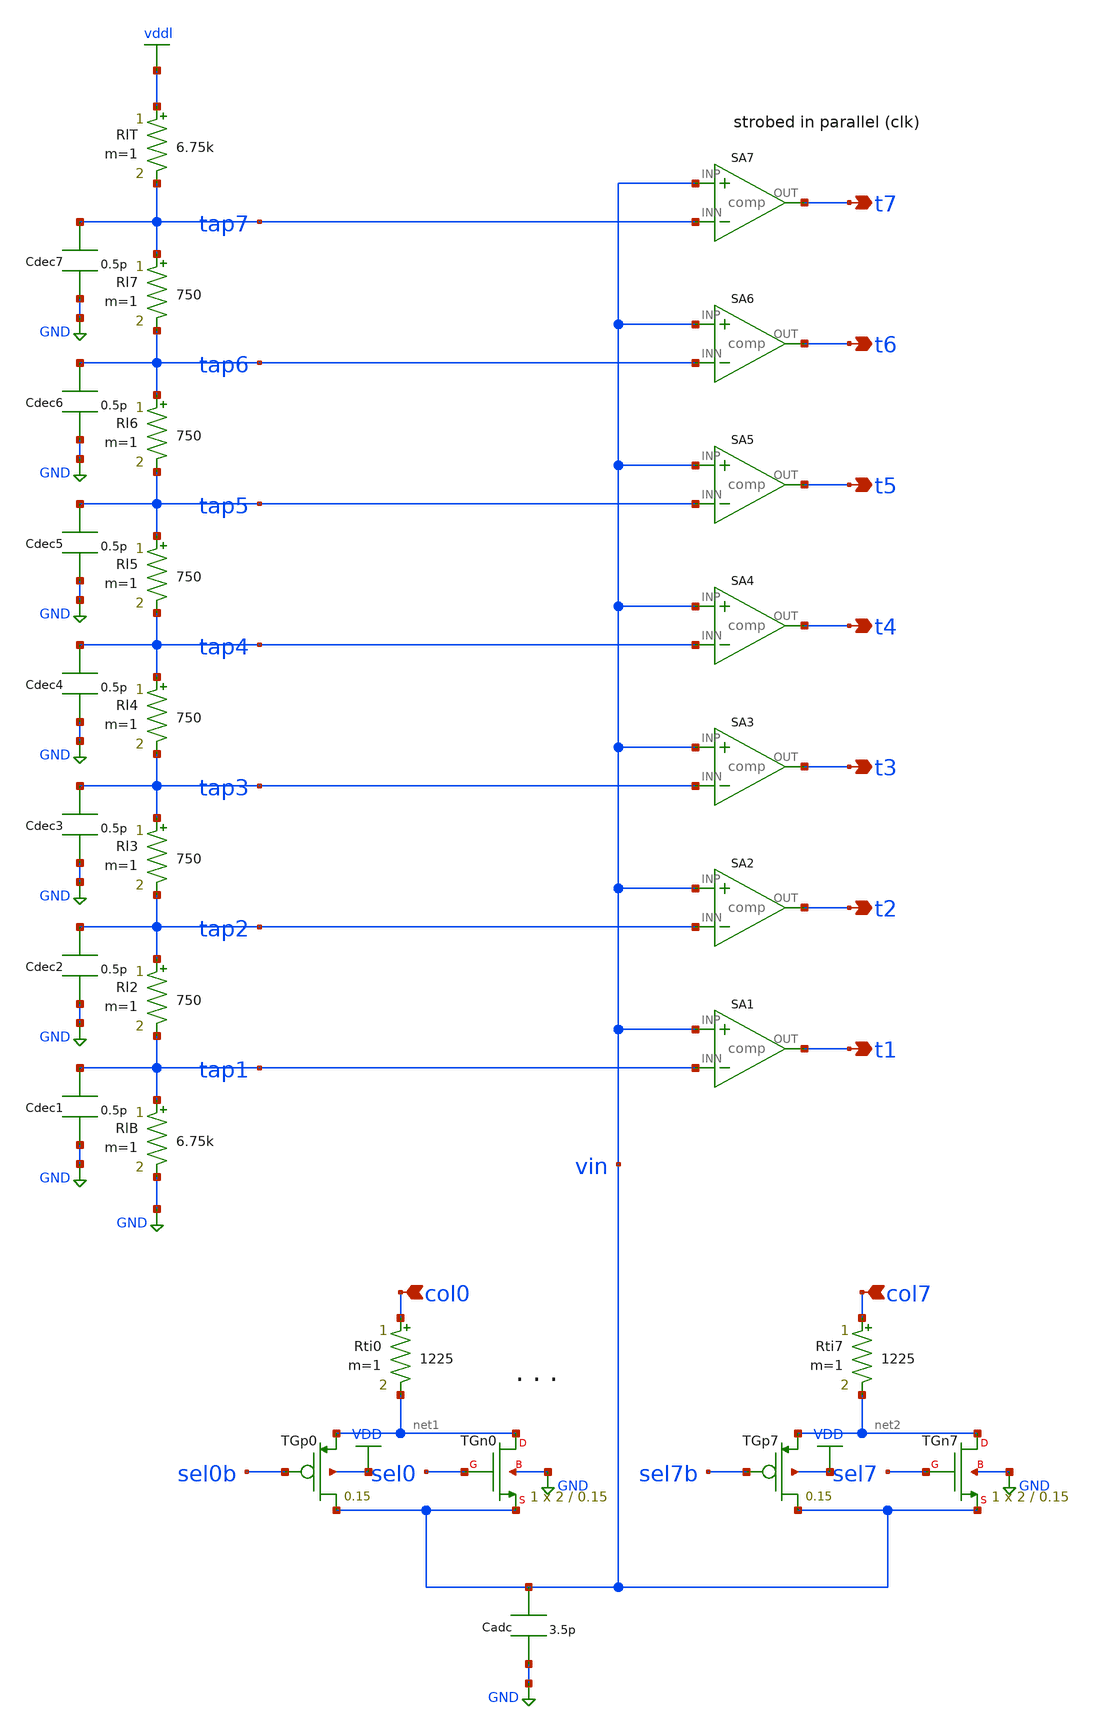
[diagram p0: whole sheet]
** sch_path: eda/hero/schematics/rram_flash_slice.sch
**.subckt rram_flash_slice t1 t2 t3 t4 t5 t6 t7 col0 col7
*.opin t1
*.opin t2
*.opin t3
*.opin t4
*.opin t5
*.opin t6
*.opin t7
*.ipin col0
*.ipin col7
RlT vddl tap7 6.75k m=1
Rl7 tap7 tap6 750 m=1
Rl6 tap6 tap5 750 m=1
Rl5 tap5 tap4 750 m=1
Rl4 tap4 tap3 750 m=1
Rl3 tap3 tap2 750 m=1
Rl2 tap2 tap1 750 m=1
RlB tap1 GND 6.75k m=1
Cdec1 tap1 GND 0.5p m=1
Cdec2 tap2 GND 0.5p m=1
Cdec3 tap3 GND 0.5p m=1
Cdec4 tap4 GND 0.5p m=1
Cdec5 tap5 GND 0.5p m=1
Cdec6 tap6 GND 0.5p m=1
Cdec7 tap7 GND 0.5p m=1
Rti0 col0 net1 1225 m=1
XTGp0 vin sel0b net1 VDD sky130_fd_pr__sky130_fd_pr__pfet_01v8 L=0.15 W=4 nrd='0.29 / W' nrs='0.29 / W'
+ sa=0 sb=0 sd=0 mult=1 m=1
XTGn0 net1 sel0 vin GND sky130_fd_pr__sky130_fd_pr__nfet_01v8 L=0.15 W=2 nrd='0.29 / W' nrs='0.29 / W'
+ sa=0 sb=0 sd=0 mult=1 m=1
Rti7 col7 net2 1225 m=1
XTGp7 vin sel7b net2 VDD sky130_fd_pr__sky130_fd_pr__pfet_01v8 L=0.15 W=4 nrd='0.29 / W' nrs='0.29 / W'
+ sa=0 sb=0 sd=0 mult=1 m=1
XTGn7 net2 sel7 vin GND sky130_fd_pr__sky130_fd_pr__nfet_01v8 L=0.15 W=2 nrd='0.29 / W' nrs='0.29 / W'
+ sa=0 sb=0 sd=0 mult=1 m=1
Cadc vin GND 3.5p m=1
**.ends
.GLOBAL vddl
.GLOBAL GND
.GLOBAL VDD
.end
